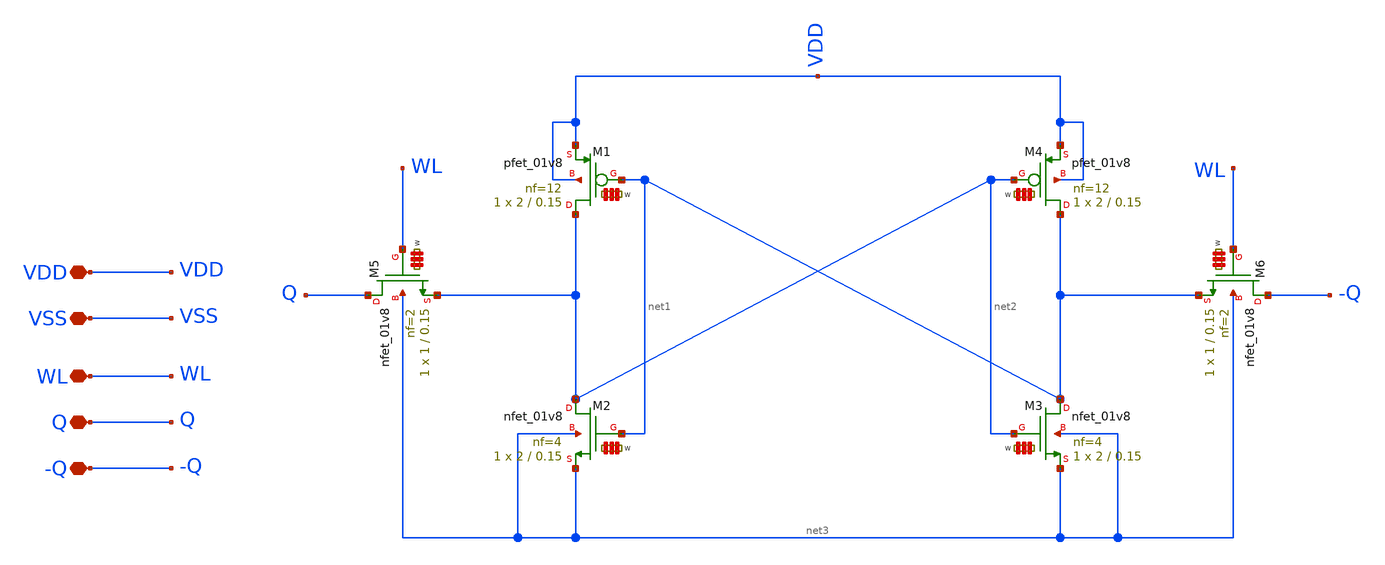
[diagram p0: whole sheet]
** sch_path: my_ip/LIB/Memory/SRAM_001_1_8_sky130A.sch
**.subckt SRAM_001_1_8_sky130A VDD VSS WL Q -Q
*.iopin VDD
*.iopin VSS
*.iopin WL
*.iopin Q
*.iopin -Q
XM1 net2 net1 VDD VDD sky130_fd_pr__pfet_01v8 L=0.15 W='2 * 12 ' nf=12 ad= as='int((12 + 2)/2) * 2 * 0.29'
+ pd='2*int((12 + 1)/2) * (2 + 0.29)' ps='2*int((12 + 2)/2) * (2 + 0.29)' nrd='0.29 / 2 / 12 ' nrs='0.29 / 2 / 12 '
+ sa=0 sb=0 sd=0 mult=1 m=1
XM2 net2 net1 net3 net3 sky130_fd_pr__nfet_01v8 L=0.15 W='2 * 4 ' nf=4 ad='int((4 + 1)/2) * 2 / 4 * 0.29'
+ as='int((4 + 2)/2) * 2 / 4 * 0.29' pd='2*int((4 + 1)/2) * (2 / 4 + 0.29)' ps='2*int((4 + 2)/2) * (2 / 4 + 0.29)'
+ nrd='0.29 / 2 ' nrs='0.29 / 2 ' sa=0 sb=0 sd=0 mult=1 m=1
XM5 Q WL net2 net3 sky130_fd_pr__nfet_01v8 L=0.15 W='1 * 2 ' nf=2 ad='int((2 + 1)/2) * 1 / 2 * 0.29'
+ as='int((2 + 2)/2) * 1 / 2 * 0.29' pd='2*int((2 + 1)/2) * (1 / 2 + 0.29)' ps='2*int((2 + 2)/2) * (1 / 2 + 0.29)'
+ nrd='0.29 / 1 ' nrs='0.29 / 1 ' sa=0 sb=0 sd=0 mult=1 m=1
XM6 -Q WL net1 net3 sky130_fd_pr__nfet_01v8 L=0.15 W='1 * 2 ' nf=2 ad='int((2 + 1)/2) * 1 / 2 * 0.29'
+ as='int((2 + 2)/2) * 1 / 2 * 0.29' pd='2*int((2 + 1)/2) * (1 / 2 + 0.29)' ps='2*int((2 + 2)/2) * (1 / 2 + 0.29)'
+ nrd='0.29 / 1 ' nrs='0.29 / 1 ' sa=0 sb=0 sd=0 mult=1 m=1
XM3 net1 net2 net3 net3 sky130_fd_pr__nfet_01v8 L=0.15 W='2 * 4 ' nf=4 ad='int((4 + 1)/2) * 2 / 4 * 0.29'
+ as='int((4 + 2)/2) * 2 / 4 * 0.29' pd='2*int((4 + 1)/2) * (2 / 4 + 0.29)' ps='2*int((4 + 2)/2) * (2 / 4 + 0.29)'
+ nrd='0.29 / 2 ' nrs='0.29 / 2 ' sa=0 sb=0 sd=0 mult=1 m=1
XM4 net1 net2 VDD VDD sky130_fd_pr__pfet_01v8 L=0.15 W='2 * 12 ' nf=12 ad= as='int((12 + 2)/2) * 2 * 0.29'
+ pd='2*int((12 + 1)/2) * (2 + 0.29)' ps='2*int((12 + 2)/2) * (2 + 0.29)' nrd='0.29 / 2 / 12 ' nrs='0.29 / 2 / 12 '
+ sa=0 sb=0 sd=0 mult=1 m=1
**.ends
.end
